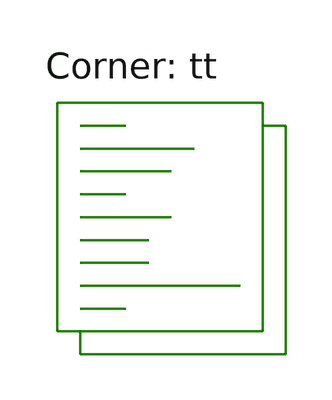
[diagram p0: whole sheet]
** sch_path: xschem/test_ring_100mV_extracted.sch
**.subckt test_ring_100mV_extracted
**** begin user architecture code
.lib $::SKYWATER_MODELS/sky130.lib.spice tt
**** end user architecture code
**.ends
**** begin user architecture code


** this experimental option enables mos model bin
** selection based on W/NF instead of W
*.option wnflag=1 savecurrents
.option gmin=1e-14 reltol=1e-3 vntol=1e-4 abstol=1e-14

v_dd DD 0 dc=0.1
v_ss SS 0 dc=0

.ic v(mdls_inv_7/IN)=0

.subckt sky130_fd_pr__nfet_01v8_lvt_62AYNZ a_n158_n550# a_n100_n638# a_100_n550# VSUBS
X0 a_100_n550# a_n100_n638# a_n158_n550# VSUBS sky130_fd_pr__nfet_01v8_lvt ad=1.6 pd=11.6 as=1.6
+ ps=11.6 w=5.5 l=1
C0 a_100_n550# a_n100_n638# 0.123f
C1 a_n100_n638# a_n158_n550# 0.123f
C2 a_100_n550# a_n158_n550# 0.301f
C3 a_100_n550# VSUBS 0.552f
C4 a_n158_n550# VSUBS 0.552f
C5 a_n100_n638# VSUBS 0.688f
.ends

.subckt sky130_fd_pr__nfet_01v8_lvt_P9XYHJ a_80_n550# a_n138_n550# a_n80_n638# VSUBS
X0 a_80_n550# a_n80_n638# a_n138_n550# VSUBS sky130_fd_pr__nfet_01v8_lvt ad=1.6 pd=11.6 as=1.6
+ ps=11.6 w=5.5 l=0.8
C0 a_n138_n550# a_n80_n638# 0.105f
C1 a_n138_n550# a_80_n550# 0.356f
C2 a_80_n550# a_n80_n638# 0.105f
C3 a_80_n550# VSUBS 0.541f
C4 a_n138_n550# VSUBS 0.541f
C5 a_n80_n638# VSUBS 0.58f
.ends

.subckt sky130_fd_pr__pfet_01v8_lvt_G2G9KE a_n138_n100# a_n80_n197# a_80_n100# w_n174_n200#  VSUBS
X0 a_80_n100# a_n80_n197# a_n138_n100# w_n174_n200# sky130_fd_pr__pfet_01v8_lvt ad=0.29 pd=2.58
+ as=0.29 ps=2.58 w=1 l=0.8
C0 a_n80_n197# w_n174_n200# 0.15f
C1 a_n80_n197# a_n138_n100# 0.0232f
C2 a_n138_n100# w_n174_n200# 0.00922f
C3 a_80_n100# a_n80_n197# 0.0232f
C4 a_80_n100# w_n174_n200# 0.00922f
C5 a_80_n100# a_n138_n100# 0.0658f
C6 a_80_n100# VSUBS 0.116f
C7 a_n138_n100# VSUBS 0.116f
C8 a_n80_n197# VSUBS 0.428f
C9 w_n174_n200# VSUBS 0.418f
.ends

.subckt sky130_fd_pr__pfet_01v8_lvt_NCVK88 a_n258_n100# a_n200_n197# a_200_n100# w_n294_n200#  VSUBS
X0 a_200_n100# a_n200_n197# a_n258_n100# w_n294_n200# sky130_fd_pr__pfet_01v8_lvt ad=0.29 pd=2.58
+ as=0.29 ps=2.58 w=1 l=2
C0 a_n200_n197# w_n294_n200# 0.276f
C1 a_n200_n197# a_200_n100# 0.0375f
C2 a_200_n100# w_n294_n200# 0.0092f
C3 a_n258_n100# a_n200_n197# 0.0375f
C4 a_n258_n100# w_n294_n200# 0.0092f
C5 a_n258_n100# a_200_n100# 0.0313f
C6 a_200_n100# VSUBS 0.125f
C7 a_n258_n100# VSUBS 0.125f
C8 a_n200_n197# VSUBS 0.924f
C9 w_n294_n200# VSUBS 0.706f
.ends

.subckt sky130_fd_pr__nfet_01v8_lvt_P34KHJ a_40_n550# a_n98_n550# a_n40_n638# VSUBS
X0 a_40_n550# a_n40_n638# a_n98_n550# VSUBS sky130_fd_pr__nfet_01v8_lvt ad=1.6 pd=11.6 as=1.6
+ ps=11.6 w=5.5 l=0.4
C0 a_n98_n550# a_n40_n638# 0.0591f
C1 a_40_n550# a_n98_n550# 0.561f
C2 a_40_n550# a_n40_n638# 0.0591f
C3 a_40_n550# VSUBS 0.516f
C4 a_n98_n550# VSUBS 0.516f
C5 a_n40_n638# VSUBS 0.364f
.ends

.subckt mdls_inv m1_2309_1084# a_2701_260# li_n14_266# IN OUT DD SS
Xsky130_fd_pr__nfet_01v8_lvt_62AYNZ_1 li_n14_266# IN SS SS sky130_fd_pr__nfet_01v8_lvt_62AYNZ
Xsky130_fd_pr__nfet_01v8_lvt_62AYNZ_0 li_n14_266# IN SS SS sky130_fd_pr__nfet_01v8_lvt_62AYNZ
Xsky130_fd_pr__nfet_01v8_lvt_P9XYHJ_4 OUT li_n14_266# IN SS sky130_fd_pr__nfet_01v8_lvt_P9XYHJ
Xsky130_fd_pr__nfet_01v8_lvt_P9XYHJ_5 OUT li_n14_266# IN SS sky130_fd_pr__nfet_01v8_lvt_P9XYHJ
Xsky130_fd_pr__nfet_01v8_lvt_P9XYHJ_6 OUT li_n14_266# IN SS sky130_fd_pr__nfet_01v8_lvt_P9XYHJ
Xsky130_fd_pr__nfet_01v8_lvt_P9XYHJ_7 OUT li_n14_266# IN SS sky130_fd_pr__nfet_01v8_lvt_P9XYHJ
Xsky130_fd_pr__pfet_01v8_lvt_G2G9KE_0 m1_2309_1084# IN OUT DD SS sky130_fd_pr__pfet_01v8_lvt_G2G9KE
Xsky130_fd_pr__pfet_01v8_lvt_G2G9KE_1 li_n14_266# OUT SS DD SS sky130_fd_pr__pfet_01v8_lvt_G2G9KE
Xsky130_fd_pr__pfet_01v8_lvt_NCVK88_0 m1_2309_1084# IN DD DD SS sky130_fd_pr__pfet_01v8_lvt_NCVK88
Xsky130_fd_pr__nfet_01v8_lvt_P34KHJ_0 m1_2309_1084# DD OUT SS sky130_fd_pr__nfet_01v8_lvt_P34KHJ
Xsky130_fd_pr__nfet_01v8_lvt_P34KHJ_1 m1_2309_1084# DD OUT SS sky130_fd_pr__nfet_01v8_lvt_P34KHJ
C0 li_n14_266# m1_2309_1084# 1f
C1 li_n14_266# DD 0.2f
C2 OUT m1_2309_1084# 0.871f
C3 DD OUT 2.36f
C4 IN m1_2309_1084# 0.542f
C5 IN DD 1.03f
C6 li_n14_266# OUT 3.06f
C7 IN li_n14_266# 1.7f
C8 IN OUT 0.925f
C9 DD m1_2309_1084# 0.407f
C10 IN SS 4.96f
C11 m1_2309_1084# SS 0.44f
C12 DD SS 5.19f
C13 OUT SS 3.17f
C14 li_n14_266# SS 2.12f
.ends


* Top level circuit ring_100mV

Xmdls_inv_0 mdls_inv_0/m1_2309_1084# SS mdls_inv_0/li_n14_266# mdls_inv_0/IN mdls_inv_1/IN  DD SS
+ mdls_inv
Xmdls_inv_1 mdls_inv_1/m1_2309_1084# SS mdls_inv_1/li_n14_266# mdls_inv_1/IN mdls_inv_8/IN  DD SS
+ mdls_inv
Xmdls_inv_2 mdls_inv_2/m1_2309_1084# SS mdls_inv_2/li_n14_266# mdls_inv_3/IN mdls_inv_5/IN  DD SS
+ mdls_inv
Xmdls_inv_3 mdls_inv_3/m1_2309_1084# SS mdls_inv_3/li_n14_266# mdls_inv_3/IN OUT DD  SS mdls_inv
Xmdls_inv_4 mdls_inv_4/m1_2309_1084# SS mdls_inv_4/li_n14_266# mdls_inv_4/IN mdls_inv_3/IN  DD SS
+ mdls_inv
Xmdls_inv_5 mdls_inv_5/m1_2309_1084# SS mdls_inv_5/li_n14_266# mdls_inv_5/IN mdls_inv_7/IN  DD SS
+ mdls_inv
Xmdls_inv_6 mdls_inv_6/m1_2309_1084# SS mdls_inv_6/li_n14_266# mdls_inv_6/IN mdls_inv_4/IN  DD SS
+ mdls_inv
Xmdls_inv_7 mdls_inv_7/m1_2309_1084# SS mdls_inv_7/li_n14_266# mdls_inv_7/IN mdls_inv_9/IN  DD SS
+ mdls_inv
Xmdls_inv_9 mdls_inv_9/m1_2309_1084# SS mdls_inv_9/li_n14_266# mdls_inv_9/IN mdls_inv_0/IN  DD SS
+ mdls_inv
Xmdls_inv_8 mdls_inv_8/m1_2309_1084# SS mdls_inv_8/li_n14_266# mdls_inv_8/IN mdls_inv_6/IN  DD SS
+ mdls_inv
C0 mdls_inv_0/li_n14_266# mdls_inv_8/IN 6.67e-19
C1 mdls_inv_1/li_n14_266# mdls_inv_0/IN 0.00123f
C2 mdls_inv_1/IN mdls_inv_8/li_n14_266# 2.12e-19
C3 mdls_inv_6/li_n14_266# mdls_inv_7/li_n14_266# 0.00692f
C4 mdls_inv_6/li_n14_266# mdls_inv_7/m1_2309_1084# 3.93e-21
C5 mdls_inv_8/IN mdls_inv_9/li_n14_266# 4.27e-20
C6 mdls_inv_6/IN mdls_inv_0/IN 0.109f
C7 mdls_inv_4/IN mdls_inv_9/IN 0.105f
C8 mdls_inv_4/li_n14_266# mdls_inv_4/IN 0.168f
C9 mdls_inv_8/m1_2309_1084# mdls_inv_0/IN 0.00136f
C10 mdls_inv_0/li_n14_266# mdls_inv_9/IN 3.03e-19
C11 mdls_inv_5/IN mdls_inv_7/li_n14_266# 3e-19
C12 mdls_inv_5/IN mdls_inv_7/m1_2309_1084# 1.09e-19
C13 mdls_inv_7/IN mdls_inv_5/m1_2309_1084# 0.0388f
C14 mdls_inv_4/IN mdls_inv_4/m1_2309_1084# 0.227f
C15 DD mdls_inv_9/m1_2309_1084# 0.00631f
C16 mdls_inv_2/li_n14_266# mdls_inv_3/m1_2309_1084# 3.93e-21
C17 mdls_inv_0/m1_2309_1084# mdls_inv_9/IN 1.29e-19
C18 mdls_inv_9/IN mdls_inv_9/li_n14_266# 0.129f
C19 mdls_inv_7/IN mdls_inv_5/li_n14_266# 0.0504f
C20 mdls_inv_2/li_n14_266# DD 0.00443f
C21 mdls_inv_1/IN mdls_inv_0/IN 0.983f
C22 mdls_inv_2/m1_2309_1084# mdls_inv_3/li_n14_266# 3.93e-21
C23 mdls_inv_6/li_n14_266# DD 0.00443f
C24 mdls_inv_0/li_n14_266# mdls_inv_1/li_n14_266# 0.00692f
C25 mdls_inv_7/li_n14_266# mdls_inv_0/IN 0.148f
C26 mdls_inv_7/m1_2309_1084# mdls_inv_0/IN 6.99e-19
C27 mdls_inv_5/IN mdls_inv_3/m1_2309_1084# 6.45e-19
C28 DD mdls_inv_8/li_n14_266# 0.00443f
C29 mdls_inv_4/IN mdls_inv_6/IN 0.0927f
C30 mdls_inv_1/m1_2309_1084# mdls_inv_0/IN 0.00194f
C31 mdls_inv_3/IN mdls_inv_3/m1_2309_1084# 0.0612f
C32 mdls_inv_5/IN DD 0.472f
C33 mdls_inv_1/li_n14_266# mdls_inv_0/m1_2309_1084# 3.93e-21
C34 mdls_inv_3/IN DD 0.593f
C35 OUT mdls_inv_3/li_n14_266# 0.222f
C36 mdls_inv_6/m1_2309_1084# mdls_inv_4/IN 0.0155f
C37 mdls_inv_6/IN mdls_inv_9/li_n14_266# 0.00101f
C38 mdls_inv_8/m1_2309_1084# mdls_inv_9/li_n14_266# 3.93e-21
C39 mdls_inv_9/m1_2309_1084# mdls_inv_8/li_n14_266# 3.93e-21
C40 mdls_inv_5/m1_2309_1084# mdls_inv_9/IN 3.31e-19
C41 mdls_inv_4/li_n14_266# mdls_inv_5/m1_2309_1084# 3.93e-21
C42 mdls_inv_0/li_n14_266# mdls_inv_1/IN 0.216f
C43 mdls_inv_7/IN mdls_inv_2/m1_2309_1084# 0.00215f
C44 mdls_inv_2/li_n14_266# mdls_inv_5/IN 0.224f
C45 DD mdls_inv_0/IN 0.453f
C46 mdls_inv_4/IN mdls_inv_7/li_n14_266# 6.67e-19
C47 mdls_inv_4/m1_2309_1084# mdls_inv_5/m1_2309_1084# 0.0129f
C48 mdls_inv_4/li_n14_266# mdls_inv_5/li_n14_266# 0.00692f
C49 mdls_inv_9/IN mdls_inv_5/li_n14_266# 0.148f
C50 mdls_inv_3/IN mdls_inv_2/li_n14_266# 4.27e-20
C51 mdls_inv_1/IN mdls_inv_0/m1_2309_1084# 0.158f
C52 mdls_inv_1/IN mdls_inv_9/li_n14_266# 0.148f
C53 mdls_inv_4/li_n14_266# mdls_inv_7/IN 9.84e-19
C54 mdls_inv_7/IN mdls_inv_9/IN 0.726f
C55 mdls_inv_0/li_n14_266# mdls_inv_1/m1_2309_1084# 3.93e-21
C56 mdls_inv_4/m1_2309_1084# mdls_inv_5/li_n14_266# 3.93e-21
C57 mdls_inv_3/IN mdls_inv_6/li_n14_266# 2.73e-19
C58 mdls_inv_7/IN mdls_inv_4/m1_2309_1084# 0.00136f
C59 mdls_inv_9/m1_2309_1084# mdls_inv_0/IN 0.0388f
C60 mdls_inv_0/m1_2309_1084# mdls_inv_1/m1_2309_1084# 0.0129f
C61 mdls_inv_3/IN mdls_inv_5/IN 0.377f
C62 mdls_inv_4/IN mdls_inv_3/m1_2309_1084# 1.37e-19
C63 mdls_inv_4/IN DD 0.439f
C64 mdls_inv_0/li_n14_266# DD 0.0034f
C65 mdls_inv_6/IN mdls_inv_7/IN 0.191f
C66 mdls_inv_8/li_n14_266# mdls_inv_0/IN 9.84e-19
C67 mdls_inv_8/IN mdls_inv_9/IN 0.179f
C68 DD mdls_inv_0/m1_2309_1084# 0.00623f
C69 DD mdls_inv_9/li_n14_266# 0.00443f
C70 mdls_inv_6/m1_2309_1084# mdls_inv_7/IN 0.00194f
C71 DD mdls_inv_3/li_n14_266# 0.00443f
C72 mdls_inv_4/li_n14_266# OUT 1.44e-19
C73 mdls_inv_8/IN mdls_inv_1/li_n14_266# 0.178f
C74 mdls_inv_4/IN mdls_inv_6/li_n14_266# 0.178f
C75 mdls_inv_7/li_n14_266# mdls_inv_7/IN 0.0233f
C76 mdls_inv_7/IN mdls_inv_7/m1_2309_1084# 0.0616f
C77 mdls_inv_4/IN mdls_inv_8/li_n14_266# 1.33e-19
C78 mdls_inv_6/IN mdls_inv_8/IN 0.097f
C79 mdls_inv_8/IN mdls_inv_8/m1_2309_1084# 0.224f
C80 mdls_inv_4/IN mdls_inv_5/IN 0.179f
C81 mdls_inv_3/IN mdls_inv_4/IN 0.0963f
C82 mdls_inv_6/m1_2309_1084# mdls_inv_8/IN 1.5e-19
C83 mdls_inv_8/li_n14_266# mdls_inv_9/li_n14_266# 0.00692f
C84 DD mdls_inv_5/m1_2309_1084# 0.00631f
C85 mdls_inv_4/li_n14_266# mdls_inv_6/IN 2.12e-19
C86 mdls_inv_6/IN mdls_inv_9/IN 0.015f
C87 mdls_inv_2/li_n14_266# mdls_inv_3/li_n14_266# 0.00692f
C88 mdls_inv_8/m1_2309_1084# mdls_inv_9/IN 0.00155f
C89 mdls_inv_8/IN mdls_inv_1/IN 0.154f
C90 DD mdls_inv_5/li_n14_266# 0.00443f
C91 mdls_inv_6/IN mdls_inv_4/m1_2309_1084# 3.18e-19
C92 mdls_inv_6/m1_2309_1084# mdls_inv_9/IN 6.45e-19
C93 DD mdls_inv_7/IN 0.483f
C94 mdls_inv_0/li_n14_266# mdls_inv_0/IN 0.0253f
C95 mdls_inv_8/IN mdls_inv_1/m1_2309_1084# 0.0155f
C96 mdls_inv_1/IN mdls_inv_9/IN 0.112f
C97 mdls_inv_5/IN mdls_inv_3/li_n14_266# 6.89e-19
C98 mdls_inv_6/IN mdls_inv_1/li_n14_266# 2.73e-19
C99 mdls_inv_3/IN mdls_inv_3/li_n14_266# 0.168f
C100 mdls_inv_0/m1_2309_1084# mdls_inv_0/IN 0.0661f
C101 mdls_inv_9/li_n14_266# mdls_inv_0/IN 0.0504f
C102 mdls_inv_7/IN mdls_inv_9/m1_2309_1084# 1.06e-19
C103 mdls_inv_7/li_n14_266# mdls_inv_9/IN 0.224f
C104 mdls_inv_9/IN mdls_inv_7/m1_2309_1084# 0.161f
C105 mdls_inv_6/IN mdls_inv_8/m1_2309_1084# 0.0189f
C106 mdls_inv_2/li_n14_266# mdls_inv_7/IN 0.148f
C107 mdls_inv_6/m1_2309_1084# mdls_inv_6/IN 0.0609f
C108 mdls_inv_5/IN mdls_inv_5/m1_2309_1084# 0.273f
C109 mdls_inv_1/IN mdls_inv_1/li_n14_266# 0.00153f
C110 mdls_inv_8/IN DD 0.431f
C111 mdls_inv_3/m1_2309_1084# mdls_inv_2/m1_2309_1084# 0.0129f
C112 mdls_inv_3/IN mdls_inv_5/m1_2309_1084# 1.06e-19
C113 mdls_inv_6/li_n14_266# mdls_inv_7/IN 0.00123f
C114 DD mdls_inv_2/m1_2309_1084# 0.00631f
C115 mdls_inv_5/IN mdls_inv_5/li_n14_266# 0.129f
C116 mdls_inv_1/IN mdls_inv_8/m1_2309_1084# 2.93e-21
C117 mdls_inv_3/IN mdls_inv_5/li_n14_266# 0.0011f
C118 mdls_inv_5/IN mdls_inv_7/IN 0.753f
C119 mdls_inv_3/IN mdls_inv_7/IN 0.211f
C120 DD mdls_inv_9/IN 0.513f
C121 mdls_inv_4/li_n14_266# DD 0.00443f
C122 mdls_inv_6/IN mdls_inv_7/li_n14_266# 4.27e-20
C123 mdls_inv_6/IN mdls_inv_7/m1_2309_1084# 0.00179f
C124 mdls_inv_8/IN mdls_inv_9/m1_2309_1084# 0.00146f
C125 OUT mdls_inv_3/m1_2309_1084# 0.0162f
C126 DD mdls_inv_4/m1_2309_1084# 0.00631f
C127 OUT DD 0.189f
C128 mdls_inv_6/m1_2309_1084# mdls_inv_7/li_n14_266# 3.93e-21
C129 mdls_inv_6/m1_2309_1084# mdls_inv_7/m1_2309_1084# 0.0129f
C130 mdls_inv_4/IN mdls_inv_3/li_n14_266# 2.12e-19
C131 mdls_inv_9/m1_2309_1084# mdls_inv_9/IN 0.273f
C132 mdls_inv_8/IN mdls_inv_6/li_n14_266# 2.12e-19
C133 mdls_inv_7/IN mdls_inv_0/IN 0.13f
C134 mdls_inv_1/li_n14_266# DD 0.0034f
C135 mdls_inv_8/IN mdls_inv_8/li_n14_266# 0.168f
C136 mdls_inv_1/IN mdls_inv_1/m1_2309_1084# 0.00406f
C137 mdls_inv_6/IN DD 0.415f
C138 mdls_inv_2/li_n14_266# OUT 9.64e-19
C139 DD mdls_inv_8/m1_2309_1084# 0.00631f
C140 mdls_inv_6/li_n14_266# mdls_inv_9/IN 6.94e-19
C141 mdls_inv_5/IN mdls_inv_2/m1_2309_1084# 0.161f
C142 mdls_inv_3/IN mdls_inv_2/m1_2309_1084# -1.23e-19
C143 mdls_inv_4/IN mdls_inv_5/m1_2309_1084# 0.00146f
C144 mdls_inv_8/li_n14_266# mdls_inv_9/IN 6.02e-19
C145 mdls_inv_6/m1_2309_1084# DD 0.00631f
C146 mdls_inv_5/IN mdls_inv_9/IN 0.113f
C147 mdls_inv_4/li_n14_266# mdls_inv_5/IN 6.02e-19
C148 mdls_inv_4/IN mdls_inv_5/li_n14_266# 4.27e-20
C149 mdls_inv_3/IN mdls_inv_4/li_n14_266# 0.0478f
C150 mdls_inv_9/m1_2309_1084# mdls_inv_8/m1_2309_1084# 0.0129f
C151 mdls_inv_5/IN mdls_inv_4/m1_2309_1084# 0.00155f
C152 mdls_inv_1/IN DD 0.571f
C153 mdls_inv_4/IN mdls_inv_7/IN 0.0308f
C154 OUT mdls_inv_5/IN 0.106f
C155 mdls_inv_8/IN mdls_inv_0/IN 0.0308f
C156 mdls_inv_3/IN mdls_inv_4/m1_2309_1084# 0.0192f
C157 mdls_inv_3/IN OUT 0.0804f
C158 mdls_inv_7/li_n14_266# DD 0.00443f
C159 DD mdls_inv_7/m1_2309_1084# 0.00631f
C160 DD mdls_inv_1/m1_2309_1084# 0.00623f
C161 mdls_inv_7/IN mdls_inv_9/li_n14_266# 5.55e-19
C162 mdls_inv_6/IN mdls_inv_6/li_n14_266# 0.168f
C163 mdls_inv_9/IN mdls_inv_0/IN 0.754f
C164 mdls_inv_1/IN mdls_inv_9/m1_2309_1084# 3.31e-19
C165 mdls_inv_6/IN mdls_inv_8/li_n14_266# 0.0478f
C166 mdls_inv_3/m1_2309_1084# DD 0.00631f
C167 mdls_inv_8/m1_2309_1084# SS 0.446f
C168 mdls_inv_6/IN SS 7.32f
C169 mdls_inv_8/li_n14_266# SS 2.62f
C170 mdls_inv_9/IN SS 7.34f
C171 mdls_inv_9/m1_2309_1084# SS 0.446f
C172 mdls_inv_9/li_n14_266# SS 2.62f
C173 mdls_inv_7/IN SS 7.36f
C174 mdls_inv_7/m1_2309_1084# SS 0.446f
C175 mdls_inv_7/li_n14_266# SS 2.62f
C176 mdls_inv_6/m1_2309_1084# SS 0.446f
C177 mdls_inv_4/IN SS 7.29f
C178 mdls_inv_6/li_n14_266# SS 2.62f
C179 mdls_inv_5/IN SS 7.64f
C180 mdls_inv_5/m1_2309_1084# SS 0.446f
C181 mdls_inv_5/li_n14_266# SS 2.62f
C182 mdls_inv_4/m1_2309_1084# SS 0.446f
C183 mdls_inv_3/IN SS 11.3f
C184 mdls_inv_4/li_n14_266# SS 2.62f
C185 mdls_inv_3/m1_2309_1084# SS 0.446f
C186 OUT SS 3.48f
C187 mdls_inv_3/li_n14_266# SS 2.62f
C188 mdls_inv_2/m1_2309_1084# SS 0.446f
C189 mdls_inv_2/li_n14_266# SS 2.62f
C190 mdls_inv_1/IN SS 7.36f
C191 mdls_inv_1/m1_2309_1084# SS 0.444f
C192 DD SS 47.3f
C193 mdls_inv_8/IN SS 7.38f
C194 mdls_inv_1/li_n14_266# SS 2.48f
C195 mdls_inv_0/IN SS 7.43f
C196 mdls_inv_0/m1_2309_1084# SS 0.444f
C197 mdls_inv_0/li_n14_266# SS 2.48f

.control
  option seed = 8
  let run = 1
  dowhile run < = 1
    save out
    tran 0.01m 50m
    write test_ring_parasitics.raw
    let run = run + 1
    reset
  end
  plot out
.endc


**** end user architecture code
.end
